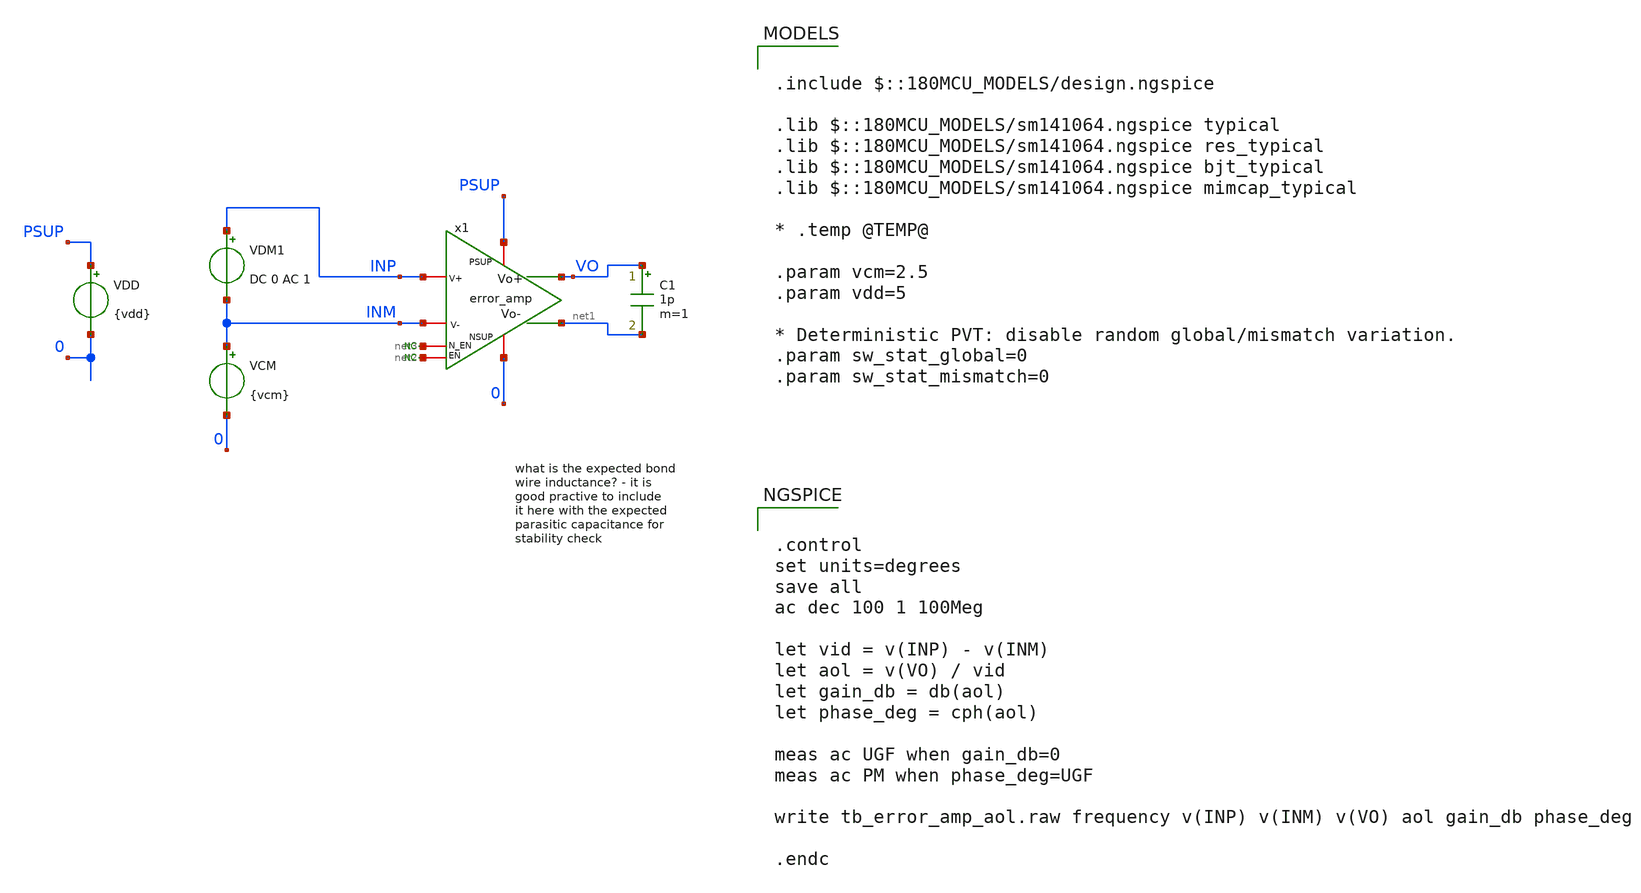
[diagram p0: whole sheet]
** sch_path: xschem/blocks/error_amp/tb_error_amp_aol.sch
**.subckt tb_error_amp_aol
VDD PSUP 0 {vdd}
VCM INM 0 {vcm}
* noconn #net2
* noconn #net3
VDM1 INP INM DC 0 AC 1
C1 VO net1 1p m=1
x1 PSUP INP INM net3 0 net2 net1 VO error_amp
**** begin user architecture code

.include $::180MCU_MODELS/design.ngspice

.lib $::180MCU_MODELS/sm141064.ngspice typical
.lib $::180MCU_MODELS/sm141064.ngspice res_typical
.lib $::180MCU_MODELS/sm141064.ngspice bjt_typical
.lib $::180MCU_MODELS/sm141064.ngspice mimcap_typical

* .temp @TEMP@

.param vcm=2.5
.param vdd=5

* Deterministic PVT: disable random global/mismatch variation.
.param sw_stat_global=0
.param sw_stat_mismatch=0



.control
set units=degrees
save all
ac dec 100 1 100Meg

let vid = v(INP) - v(INM)
let aol = v(VO) / vid
let gain_db = db(aol)
let phase_deg = cph(aol)

meas ac UGF when gain_db=0
meas ac PM when phase_deg=UGF

write tb_error_amp_aol.raw frequency v(INP) v(INM) v(VO) aol gain_db phase_deg

.endc


**** end user architecture code
**.ends

* expanding   symbol:  blocks/error_amp/error_amp.sym # of pins=8
** sym_path: xschem/blocks/error_amp/error_amp.sym
** sch_path: xschem/blocks/error_amp/error_amp.sch
.subckt error_amp PSUP V+ V- N_EN NSUP EN Vo- Vo+
*.ipin PSUP
*.ipin NSUP
*.ipin N_EN
*.ipin EN
*.ipin V+
*.ipin V-
*.opin Vo-
*.opin Vo+
XM5 AA1 vb1 PSUP PSUP pfet_06v0 L=4u W=2u nf=4 ad='int((nf+1)/2) * W/nf * 0.18u' as='int((nf+2)/2) * W/nf * 0.18u'
+ pd='2*int((nf+1)/2) * (W/nf + 0.18u)' ps='2*int((nf+2)/2) * (W/nf + 0.18u)' nrd='0.18u / W' nrs='0.18u / W'
+ sa=0 sb=0 sd=0 m=2
XM6 AA2 vb1 PSUP PSUP pfet_06v0 L=4u W=2u nf=4 ad='int((nf+1)/2) * W/nf * 0.18u' as='int((nf+2)/2) * W/nf * 0.18u'
+ pd='2*int((nf+1)/2) * (W/nf + 0.18u)' ps='2*int((nf+2)/2) * (W/nf + 0.18u)' nrd='0.18u / W' nrs='0.18u / W'
+ sa=0 sb=0 sd=0 m=2
* noconn N_EN
* noconn EN
XM1 AA4 V- AA5 NSUP nfet_06v0 L=2u W=4u nf=5 ad='int((nf+1)/2) * W/nf * 0.18u' as='int((nf+2)/2) * W/nf * 0.18u'
+ pd='2*int((nf+1)/2) * (W/nf + 0.18u)' ps='2*int((nf+2)/2) * (W/nf + 0.18u)' nrd='0.18u / W' nrs='0.18u / W'
+ sa=0 sb=0 sd=0 m=4
XM4 mirror mirror NSUP NSUP nfet_06v0 L=4u W=2u nf=2 ad='int((nf+1)/2) * W/nf * 0.18u' as='int((nf+2)/2) * W/nf * 0.18u'
+ pd='2*int((nf+1)/2) * (W/nf + 0.18u)' ps='2*int((nf+2)/2) * (W/nf + 0.18u)' nrd='0.18u / W' nrs='0.18u / W'
+ sa=0 sb=0 sd=0 m=1
I0 vb2 mirror 1u
XM7 AA5 mirror NSUP NSUP nfet_06v0 L=4u W=2u nf=4 ad='int((nf+1)/2) * W/nf * 0.18u' as='int((nf+2)/2) * W/nf * 0.18u'
+ pd='2*int((nf+1)/2) * (W/nf + 0.18u)' ps='2*int((nf+2)/2) * (W/nf + 0.18u)' nrd='0.18u / W' nrs='0.18u / W'
+ sa=0 sb=0 sd=0 m=2
XM3 vb1 vb1 PSUP PSUP pfet_06v0 L=4u W=2u nf=1 ad='int((nf+1)/2) * W/nf * 0.18u' as='int((nf+2)/2) * W/nf * 0.18u'
+ pd='2*int((nf+1)/2) * (W/nf + 0.18u)' ps='2*int((nf+2)/2) * (W/nf + 0.18u)' nrd='0.18u / W' nrs='0.18u / W'
+ sa=0 sb=0 sd=0 m=2
XM8 Vo+ vb2 AA1 AA1 pfet_06v0 L=4u W=2u nf=4 ad='int((nf+1)/2) * W/nf * 0.18u' as='int((nf+2)/2) * W/nf * 0.18u'
+ pd='2*int((nf+1)/2) * (W/nf + 0.18u)' ps='2*int((nf+2)/2) * (W/nf + 0.18u)' nrd='0.18u / W' nrs='0.18u / W'
+ sa=0 sb=0 sd=0 m=2
XM9 Vo- vb2 AA2 AA2 pfet_06v0 L=4u W=2u nf=4 ad='int((nf+1)/2) * W/nf * 0.18u' as='int((nf+2)/2) * W/nf * 0.18u'
+ pd='2*int((nf+1)/2) * (W/nf + 0.18u)' ps='2*int((nf+2)/2) * (W/nf + 0.18u)' nrd='0.18u / W' nrs='0.18u / W'
+ sa=0 sb=0 sd=0 m=2
XM10 vb2 vb2 vb1 vb1 pfet_06v0 L=4u W=2u nf=1 ad='int((nf+1)/2) * W/nf * 0.18u' as='int((nf+2)/2) * W/nf * 0.18u'
+ pd='2*int((nf+1)/2) * (W/nf + 0.18u)' ps='2*int((nf+2)/2) * (W/nf + 0.18u)' nrd='0.18u / W' nrs='0.18u / W'
+ sa=0 sb=0 sd=0 m=2
XM2 AA3 V+ AA5 NSUP nfet_06v0 L=2u W=4u nf=5 ad='int((nf+1)/2) * W/nf * 0.18u' as='int((nf+2)/2) * W/nf * 0.18u'
+ pd='2*int((nf+1)/2) * (W/nf + 0.18u)' ps='2*int((nf+2)/2) * (W/nf + 0.18u)' nrd='0.18u / W' nrs='0.18u / W'
+ sa=0 sb=0 sd=0 m=4
XM11 Vo+ vb2 AA3 AA3 nfet_06v0 L=4u W=2u nf=4 ad='int((nf+1)/2) * W/nf * 0.18u' as='int((nf+2)/2) * W/nf * 0.18u'
+ pd='2*int((nf+1)/2) * (W/nf + 0.18u)' ps='2*int((nf+2)/2) * (W/nf + 0.18u)' nrd='0.18u / W' nrs='0.18u / W'
+ sa=0 sb=0 sd=0 m=2
XM12 Vo- vb2 AA4 AA4 nfet_06v0 L=4u W=2u nf=4 ad='int((nf+1)/2) * W/nf * 0.18u' as='int((nf+2)/2) * W/nf * 0.18u'
+ pd='2*int((nf+1)/2) * (W/nf + 0.18u)' ps='2*int((nf+2)/2) * (W/nf + 0.18u)' nrd='0.18u / W' nrs='0.18u / W'
+ sa=0 sb=0 sd=0 m=2
.ends

.end
